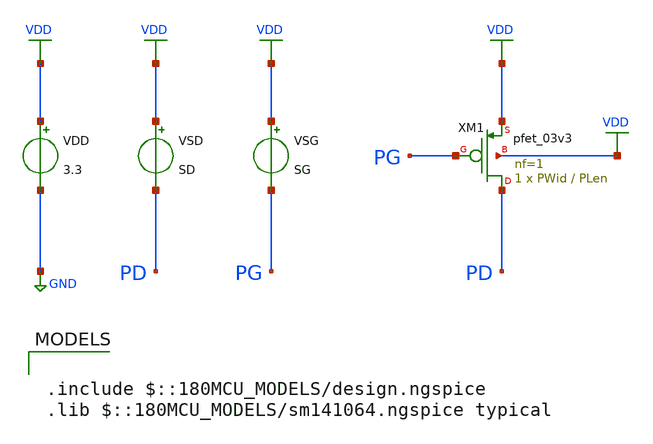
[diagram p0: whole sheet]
** sch_path: Design_Files/IC Design/Schematic/Gm_Id/PMOS_Gm_Id.sch
**.subckt PMOS_Gm_Id
XM1 PD PG VDD VDD pfet_03v3 L=PLen W=PWid nf=1 ad='int((nf+1)/2) * W/nf * 0.18u' as='int((nf+2)/2) * W/nf * 0.18u'
+ pd='2*int((nf+1)/2) * (W/nf + 0.18u)' ps='2*int((nf+2)/2) * (W/nf + 0.18u)' nrd='0.18u / W' nrs='0.18u / W'
+ sa=0 sb=0 sd=0 m=1
VSG VDD PG SG
VSD VDD PD SD
.save i(vsd)
VDD VDD GND 3.3
**** begin user architecture code



.param PWid=10u
.param PLen=1u
.param SG=0
.param SD=1.65

.control

shell mkdir -p /foss/designs/ecg_acquisition_ic/Measurement_Results/IC_Simulation/Gm_Id/PMOS_Gm_Id/

set wr_vecnames
set wr_singlescale

* =========================================================
* PMOS gm/Id 2D DC sweep
* W fixed at 10u
* Sweep VSG and VSD
* Export VSG, VSD, ID, ID/W for MATLAB
* =========================================================

alterparam PLen = 0.28u
reset
save all
dc VSG 0 3.3 0.01 VSD 0.05 3.3 0.05
let vsg_out = v(vdd)-v(pg)
let vsd_out = v(vdd)-v(pd)
let id = abs(vsd#branch)
let id_w = id/10e-6
wrdata
+ /foss/designs/ecg_acquisition_ic/Measurement_Results/IC_Simulation/Gm_Id/PMOS_Gm_Id/pmos_L0p28u_W10u.txt vsg_out vsd_out id id_w

alterparam PLen = 0.5u
reset
save all
dc VSG 0 3.3 0.01 VSD 0.05 3.3 0.05
let vsg_out = v(vdd)-v(pg)
let vsd_out = v(vdd)-v(pd)
let id = abs(vsd#branch)
let id_w = id/10e-6
wrdata
+ /foss/designs/ecg_acquisition_ic/Measurement_Results/IC_Simulation/Gm_Id/PMOS_Gm_Id/pmos_L0p5u_W10u.txt vsg_out vsd_out id id_w

alterparam PLen = 1u
reset
save all
dc VSG 0 3.3 0.01 VSD 0.05 3.3 0.05
let vsg_out = v(vdd)-v(pg)
let vsd_out = v(vdd)-v(pd)
let id = abs(vsd#branch)
let id_w = id/10e-6
wrdata
+ /foss/designs/ecg_acquisition_ic/Measurement_Results/IC_Simulation/Gm_Id/PMOS_Gm_Id/pmos_L1u_W10u.txt vsg_out vsd_out id id_w

alterparam PLen = 1.5u
reset
save all
dc VSG 0 3.3 0.01 VSD 0.05 3.3 0.05
let vsg_out = v(vdd)-v(pg)
let vsd_out = v(vdd)-v(pd)
let id = abs(vsd#branch)
let id_w = id/10e-6
wrdata
+ /foss/designs/ecg_acquisition_ic/Measurement_Results/IC_Simulation/Gm_Id/PMOS_Gm_Id/pmos_L1p5u_W10u.txt vsg_out vsd_out id id_w

alterparam PLen = 2u
reset
save all
dc VSG 0 3.3 0.01 VSD 0.05 3.3 0.05
let vsg_out = v(vdd)-v(pg)
let vsd_out = v(vdd)-v(pd)
let id = abs(vsd#branch)
let id_w = id/10e-6
wrdata
+ /foss/designs/ecg_acquisition_ic/Measurement_Results/IC_Simulation/Gm_Id/PMOS_Gm_Id/pmos_L2u_W10u.txt vsg_out vsd_out id id_w

alterparam PLen = 3u
reset
save all
dc VSG 0 3.3 0.01 VSD 0.05 3.3 0.05
let vsg_out = v(vdd)-v(pg)
let vsd_out = v(vdd)-v(pd)
let id = abs(vsd#branch)
let id_w = id/10e-6
wrdata
+ /foss/designs/ecg_acquisition_ic/Measurement_Results/IC_Simulation/Gm_Id/PMOS_Gm_Id/pmos_L3u_W10u.txt vsg_out vsd_out id id_w

.endc



.include $::180MCU_MODELS/design.ngspice
.lib $::180MCU_MODELS/sm141064.ngspice typical

**** end user architecture code
**.ends
.GLOBAL VDD
.GLOBAL GND
.end
